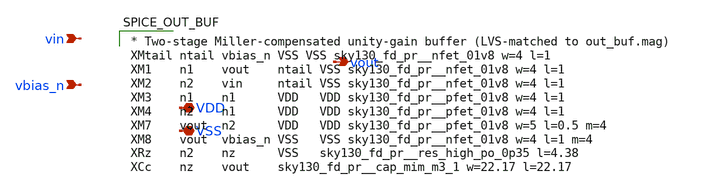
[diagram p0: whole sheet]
** sch_path: bvm_analog_tapeout/analog/out_buf/xschem/out_buf.sch
**.subckt out_buf vin vout vbias_n VDD VSS
*.ipin vin
*.opin vout
*.ipin vbias_n
*.iopin VDD
*.iopin VSS
**** begin user architecture code

* Two-stage Miller-compensated unity-gain buffer (LVS-matched to out_buf.mag)
XMtail ntail vbias_n VSS VSS sky130_fd_pr__nfet_01v8 w=4 l=1
XM1    n1    vout    ntail VSS sky130_fd_pr__nfet_01v8 w=4 l=1
XM2    n2    vin     ntail VSS sky130_fd_pr__nfet_01v8 w=4 l=1
XM3    n1    n1      VDD   VDD sky130_fd_pr__pfet_01v8 w=4 l=1
XM4    n2    n1      VDD   VDD sky130_fd_pr__pfet_01v8 w=4 l=1
XM7    vout  n2      VDD   VDD sky130_fd_pr__pfet_01v8 w=5 l=0.5 m=4
XM8    vout  vbias_n VSS   VSS sky130_fd_pr__nfet_01v8 w=4 l=1 m=4
XRz    n2    nz      VSS   sky130_fd_pr__res_high_po_0p35 l=4.38
XCc    nz    vout    sky130_fd_pr__cap_mim_m3_1 w=22.17 l=22.17

**** end user architecture code
**.ends
.end
